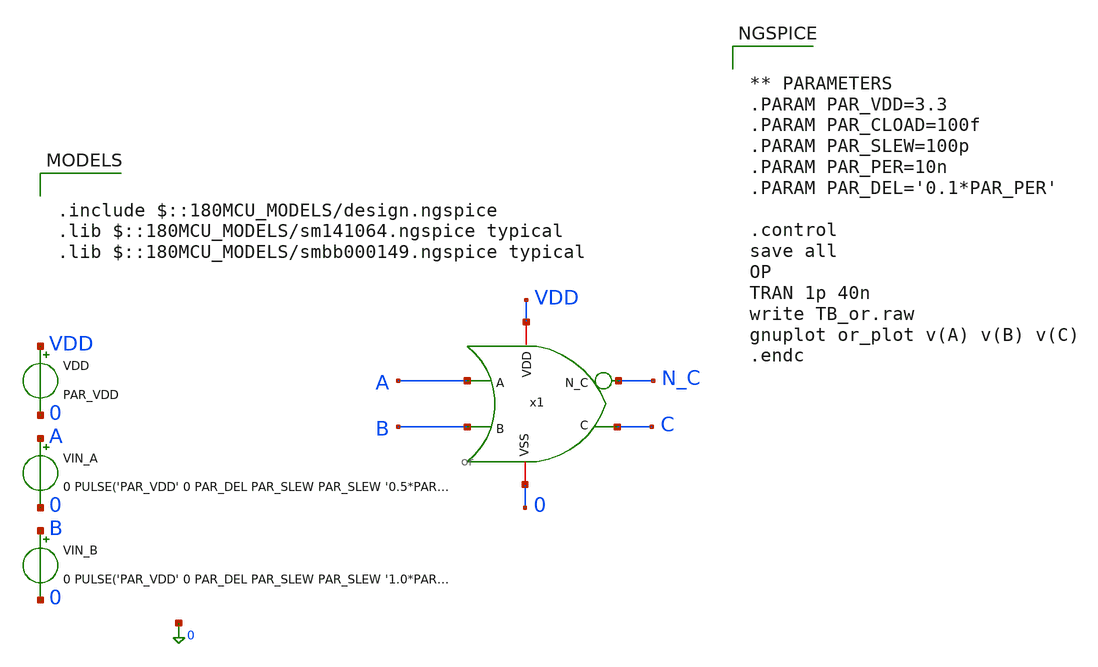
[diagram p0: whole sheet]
** sch_path: schematics/logic-gates/or/or_tb.sch
**.subckt or_tb
VIN_A A 0 0 PULSE('PAR_VDD' 0 PAR_DEL PAR_SLEW PAR_SLEW '0.5*PAR_PER' '1.0*PAR_PER')
VDD VDD 0 PAR_VDD
x1 A B N_C C VDD 0 or
VIN_B B 0 0 PULSE('PAR_VDD' 0 PAR_DEL PAR_SLEW PAR_SLEW '1.0*PAR_PER' '2.0*PAR_PER')
**** begin user architecture code

.include $::180MCU_MODELS/design.ngspice
.lib $::180MCU_MODELS/sm141064.ngspice typical
.lib $::180MCU_MODELS/smbb000149.ngspice typical



** PARAMETERS
.PARAM PAR_VDD=3.3
.PARAM PAR_CLOAD=100f
.PARAM PAR_SLEW=100p
.PARAM PAR_PER=10n
.PARAM PAR_DEL='0.1*PAR_PER'

.control
save all
OP
TRAN 1p 40n
write TB_or.raw
gnuplot or_plot v(A) v(B) v(C)
.endc



**** end user architecture code
**.ends

* expanding   symbol:  schematics/logic-gates/or/or.sym # of pins=6
** sym_path: schematics/logic-gates/or/or.sym
** sch_path: schematics/logic-gates/or/or.sch
.subckt or A B N_C C VDD VSS
*.ipin A
*.ipin B
*.opin N_C
*.opin C
*.iopin VDD
*.iopin VSS
XM1 N_C A VSS VSS nfet_03v3 L=0.28u W=0.22u nf=1 ad='int((nf+1)/2) * W/nf * 0.18u' as='int((nf+2)/2) * W/nf * 0.18u'
+ pd='2*int((nf+1)/2) * (W/nf + 0.18u)' ps='2*int((nf+2)/2) * (W/nf + 0.18u)' nrd='0.18u / W' nrs='0.18u / W'
+ sa=0 sb=0 sd=0 m=1
XM2 net1 B VDD VDD pfet_03v3 L=0.28u W=0.22u nf=1 ad='int((nf+1)/2) * W/nf * 0.18u' as='int((nf+2)/2) * W/nf * 0.18u'
+ pd='2*int((nf+1)/2) * (W/nf + 0.18u)' ps='2*int((nf+2)/2) * (W/nf + 0.18u)' nrd='0.18u / W' nrs='0.18u / W'
+ sa=0 sb=0 sd=0 m=1
XM3 N_C B VSS VSS nfet_03v3 L=0.28u W=0.22u nf=1 ad='int((nf+1)/2) * W/nf * 0.18u' as='int((nf+2)/2) * W/nf * 0.18u'
+ pd='2*int((nf+1)/2) * (W/nf + 0.18u)' ps='2*int((nf+2)/2) * (W/nf + 0.18u)' nrd='0.18u / W' nrs='0.18u / W'
+ sa=0 sb=0 sd=0 m=1
XM4 N_C A net1 VDD pfet_03v3 L=0.28u W=0.22u nf=1 ad='int((nf+1)/2) * W/nf * 0.18u' as='int((nf+2)/2) * W/nf * 0.18u'
+ pd='2*int((nf+1)/2) * (W/nf + 0.18u)' ps='2*int((nf+2)/2) * (W/nf + 0.18u)' nrd='0.18u / W' nrs='0.18u / W'
+ sa=0 sb=0 sd=0 m=1
XM5 C N_C VSS VSS nfet_03v3 L=0.28u W=0.22u nf=1 ad='int((nf+1)/2) * W/nf * 0.18u' as='int((nf+2)/2) * W/nf * 0.18u'
+ pd='2*int((nf+1)/2) * (W/nf + 0.18u)' ps='2*int((nf+2)/2) * (W/nf + 0.18u)' nrd='0.18u / W' nrs='0.18u / W'
+ sa=0 sb=0 sd=0 m=1
XM6 C N_C VDD VDD pfet_03v3 L=0.28u W=0.22u nf=1 ad='int((nf+1)/2) * W/nf * 0.18u' as='int((nf+2)/2) * W/nf * 0.18u'
+ pd='2*int((nf+1)/2) * (W/nf + 0.18u)' ps='2*int((nf+2)/2) * (W/nf + 0.18u)' nrd='0.18u / W' nrs='0.18u / W'
+ sa=0 sb=0 sd=0 m=1
.ends

.end
